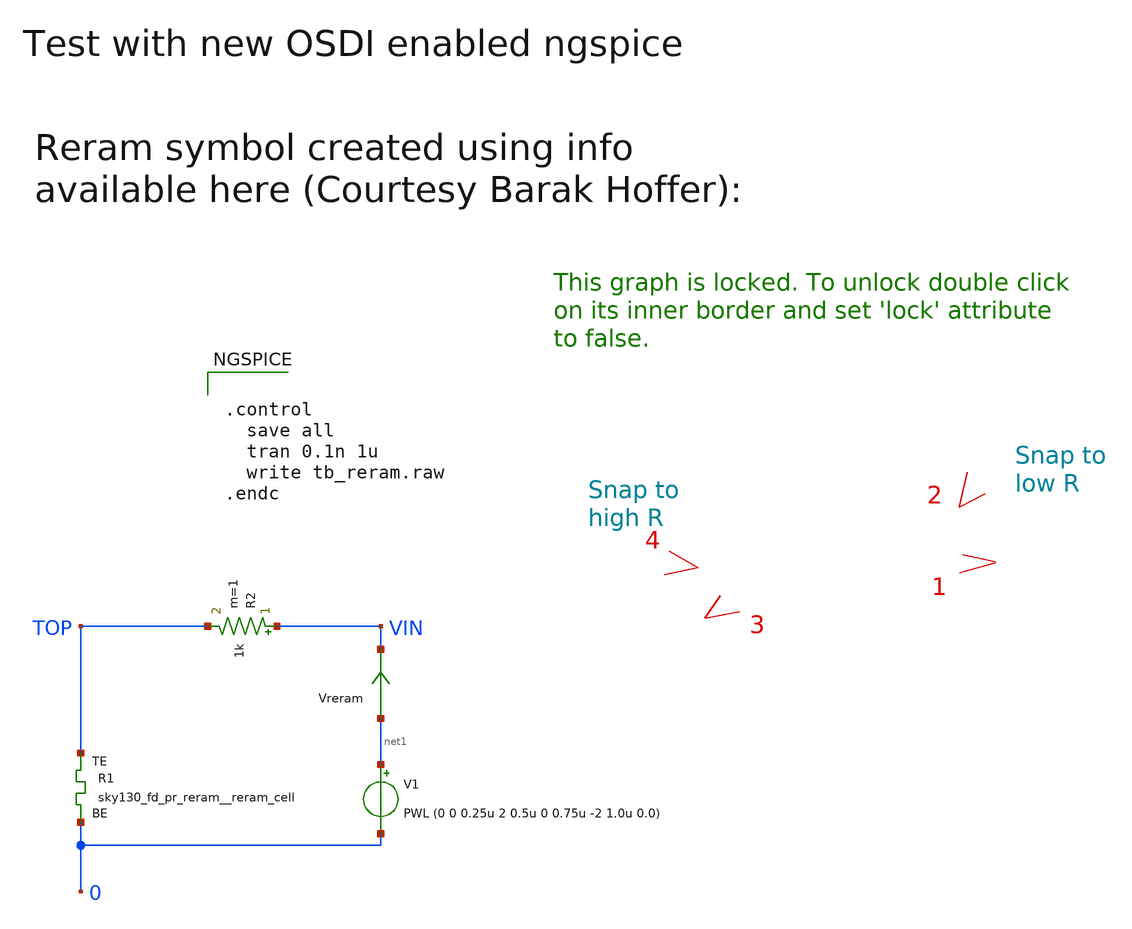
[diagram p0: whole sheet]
** sch_path: sky130_tests/tb_reram.sch
* Copyright 2021 Stefan Frederik Schippers
* Licensed under the Apache License, Version 2.0 (the "License");
* you may not use this file except in compliance with the License.
* You may obtain a copy of the License at
* https://www.apache.org/licenses/LICENSE-2.0
* Unless required by applicable law or agreed to in writing, software
* distributed under the License is distributed on an "AS IS" BASIS,
* WITHOUT WARRANTIES OR CONDITIONS OF ANY KIND, either express or implied.
* See the License for the specific language governing permissions and
* limitations under the License.
**.subckt tb_reram
V1 net1 0 PWL (0 0 0.25u 2 0.5u 0 0.75u -2 1.0u 0.0)
R1 0 TOP sky130_fd_pr_reram__reram_cell m=1
Vreram net1 VIN 0
.save i(vreram)
R2 VIN TOP 1k m=1
**** begin user architecture code


.control
  save all
  tran 0.1n 1u
  write tb_reram.raw
.endc



**** end user architecture code
**.ends
**** begin user architecture code
.model rram2_model rram2 rram2_params.scs
**** end user architecture code
.end
